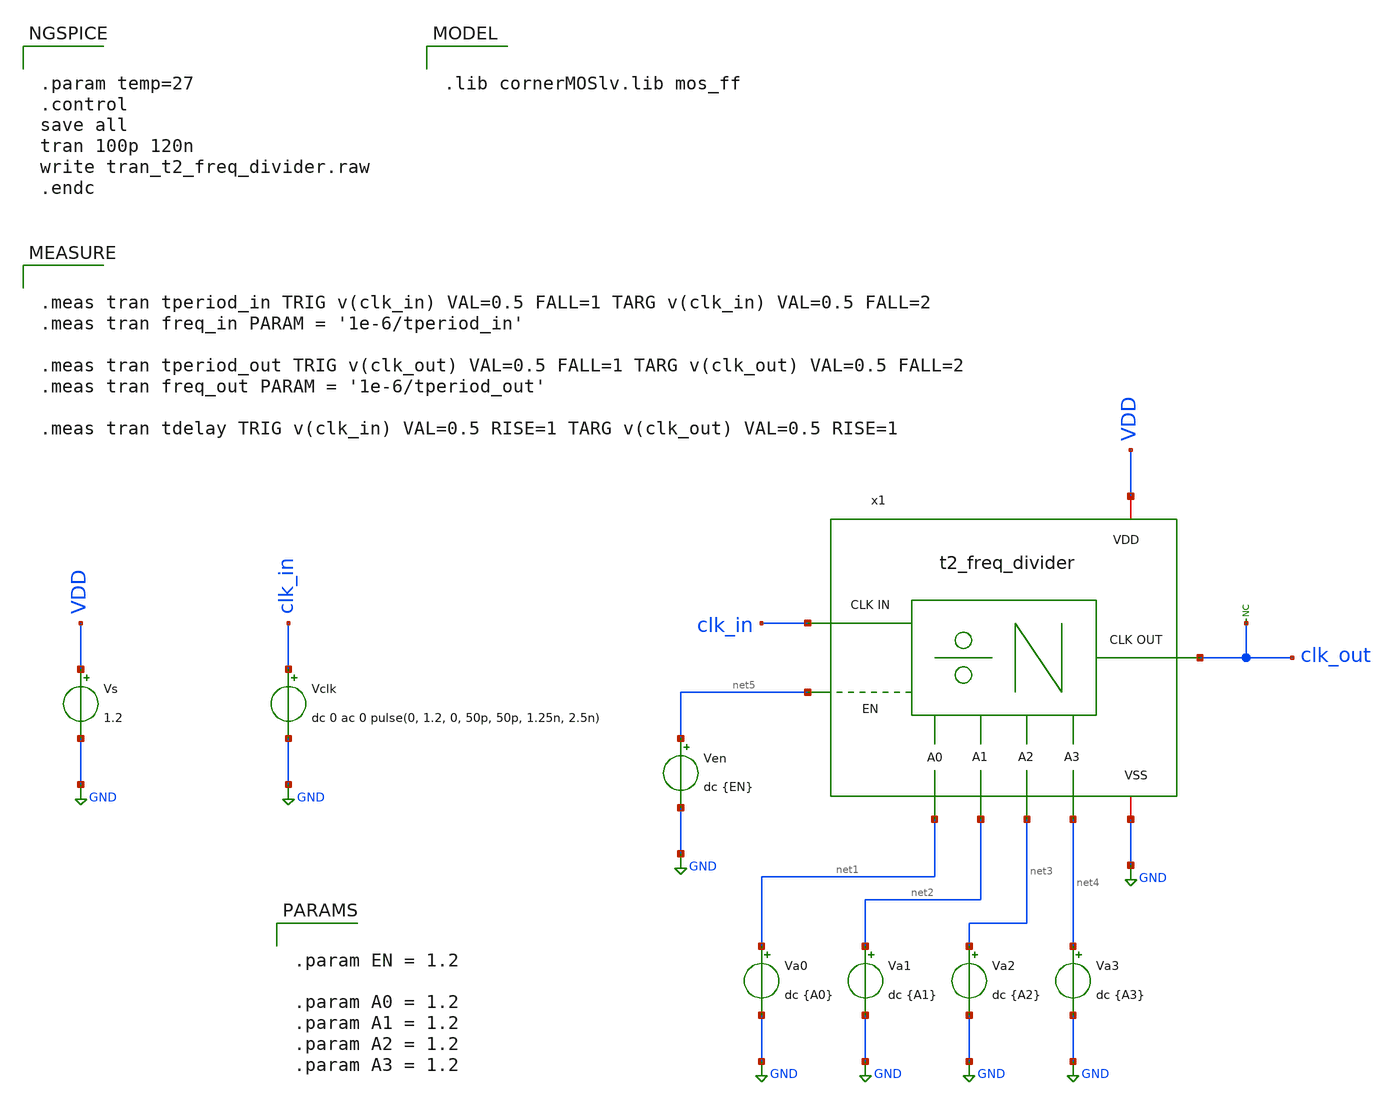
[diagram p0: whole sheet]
** sch_path: Team 2 Design/design_data/xschem/t2_freq_divider_tb.sch
**.subckt t2_freq_divider_tb
Vs VDD GND 1.2
Vclk clk_in GND dc 0 ac 0 pulse(0, 1.2, 0, 50p, 50p, 1.25n, 2.5n)
x1 VDD GND clk_in net5 net1 net2 net3 net4 clk_out t2_freq_divider
* noconn clk_out
Ven net5 GND dc {EN}
Va0 net1 GND dc {A0}
Va1 net2 GND dc {A1}
Va2 net3 GND dc {A2}
Va3 net4 GND dc {A3}
**** begin user architecture code


.param temp=27
.control
save all
tran 100p 120n
write tran_t2_freq_divider.raw
.endc



.lib cornerMOSlv.lib mos_ff



.meas tran tperiod_in TRIG v(clk_in) VAL=0.5 FALL=1 TARG v(clk_in) VAL=0.5 FALL=2
.meas tran freq_in PARAM = '1e-6/tperiod_in'

.meas tran tperiod_out TRIG v(clk_out) VAL=0.5 FALL=1 TARG v(clk_out) VAL=0.5 FALL=2
.meas tran freq_out PARAM = '1e-6/tperiod_out'

.meas tran tdelay TRIG v(clk_in) VAL=0.5 RISE=1 TARG v(clk_out) VAL=0.5 RISE=1




.param EN = 1.2

.param A0 = 1.2
.param A1 = 1.2
.param A2 = 1.2
.param A3 = 1.2


**** end user architecture code
**.ends
.GLOBAL GND
.end
